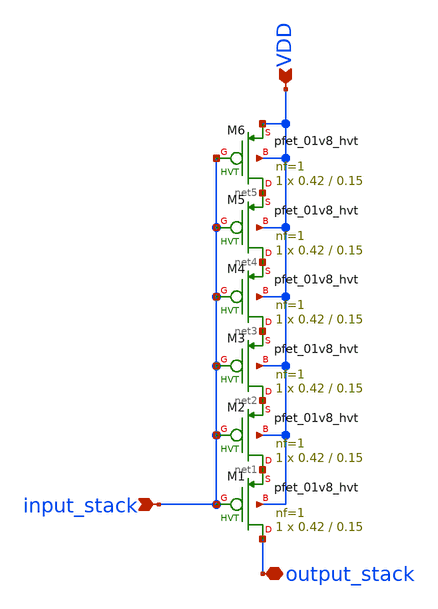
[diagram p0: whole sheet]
** sch_path: hgu/xschem/hgu_pfet_hvt_stack_in_delay.sch
**.subckt hgu_pfet_hvt_stack_in_delay VDD input_stack output_stack
*.ipin VDD
*.ipin input_stack
*.iopin output_stack
XM1 output_stack input_stack net1 VDD sky130_fd_pr__pfet_01v8_hvt L=0.15 W=0.42 nf=1 ad='int((nf+1)/2) * W/nf * 0.29'
+ as='int((nf+2)/2) * W/nf * 0.29' pd='2*int((nf+1)/2) * (W/nf + 0.29)' ps='2*int((nf+2)/2) * (W/nf + 0.29)'
+ nrd='0.29 / W' nrs='0.29 / W' sa=0 sb=0 sd=0 mult=1 m=1
XM2 net1 input_stack net2 VDD sky130_fd_pr__pfet_01v8_hvt L=0.15 W=0.42 nf=1 ad='int((nf+1)/2) * W/nf * 0.29'
+ as='int((nf+2)/2) * W/nf * 0.29' pd='2*int((nf+1)/2) * (W/nf + 0.29)' ps='2*int((nf+2)/2) * (W/nf + 0.29)'
+ nrd='0.29 / W' nrs='0.29 / W' sa=0 sb=0 sd=0 mult=1 m=1
XM3 net2 input_stack net3 VDD sky130_fd_pr__pfet_01v8_hvt L=0.15 W=0.42 nf=1 ad='int((nf+1)/2) * W/nf * 0.29'
+ as='int((nf+2)/2) * W/nf * 0.29' pd='2*int((nf+1)/2) * (W/nf + 0.29)' ps='2*int((nf+2)/2) * (W/nf + 0.29)'
+ nrd='0.29 / W' nrs='0.29 / W' sa=0 sb=0 sd=0 mult=1 m=1
XM4 net3 input_stack net4 VDD sky130_fd_pr__pfet_01v8_hvt L=0.15 W=0.42 nf=1 ad='int((nf+1)/2) * W/nf * 0.29'
+ as='int((nf+2)/2) * W/nf * 0.29' pd='2*int((nf+1)/2) * (W/nf + 0.29)' ps='2*int((nf+2)/2) * (W/nf + 0.29)'
+ nrd='0.29 / W' nrs='0.29 / W' sa=0 sb=0 sd=0 mult=1 m=1
XM5 net4 input_stack net5 VDD sky130_fd_pr__pfet_01v8_hvt L=0.15 W=0.42 nf=1 ad='int((nf+1)/2) * W/nf * 0.29'
+ as='int((nf+2)/2) * W/nf * 0.29' pd='2*int((nf+1)/2) * (W/nf + 0.29)' ps='2*int((nf+2)/2) * (W/nf + 0.29)'
+ nrd='0.29 / W' nrs='0.29 / W' sa=0 sb=0 sd=0 mult=1 m=1
XM6 net5 input_stack VDD VDD sky130_fd_pr__pfet_01v8_hvt L=0.15 W=0.42 nf=1 ad='int((nf+1)/2) * W/nf * 0.29'
+ as='int((nf+2)/2) * W/nf * 0.29' pd='2*int((nf+1)/2) * (W/nf + 0.29)' ps='2*int((nf+2)/2) * (W/nf + 0.29)'
+ nrd='0.29 / W' nrs='0.29 / W' sa=0 sb=0 sd=0 mult=1 m=1
**.ends
.end
